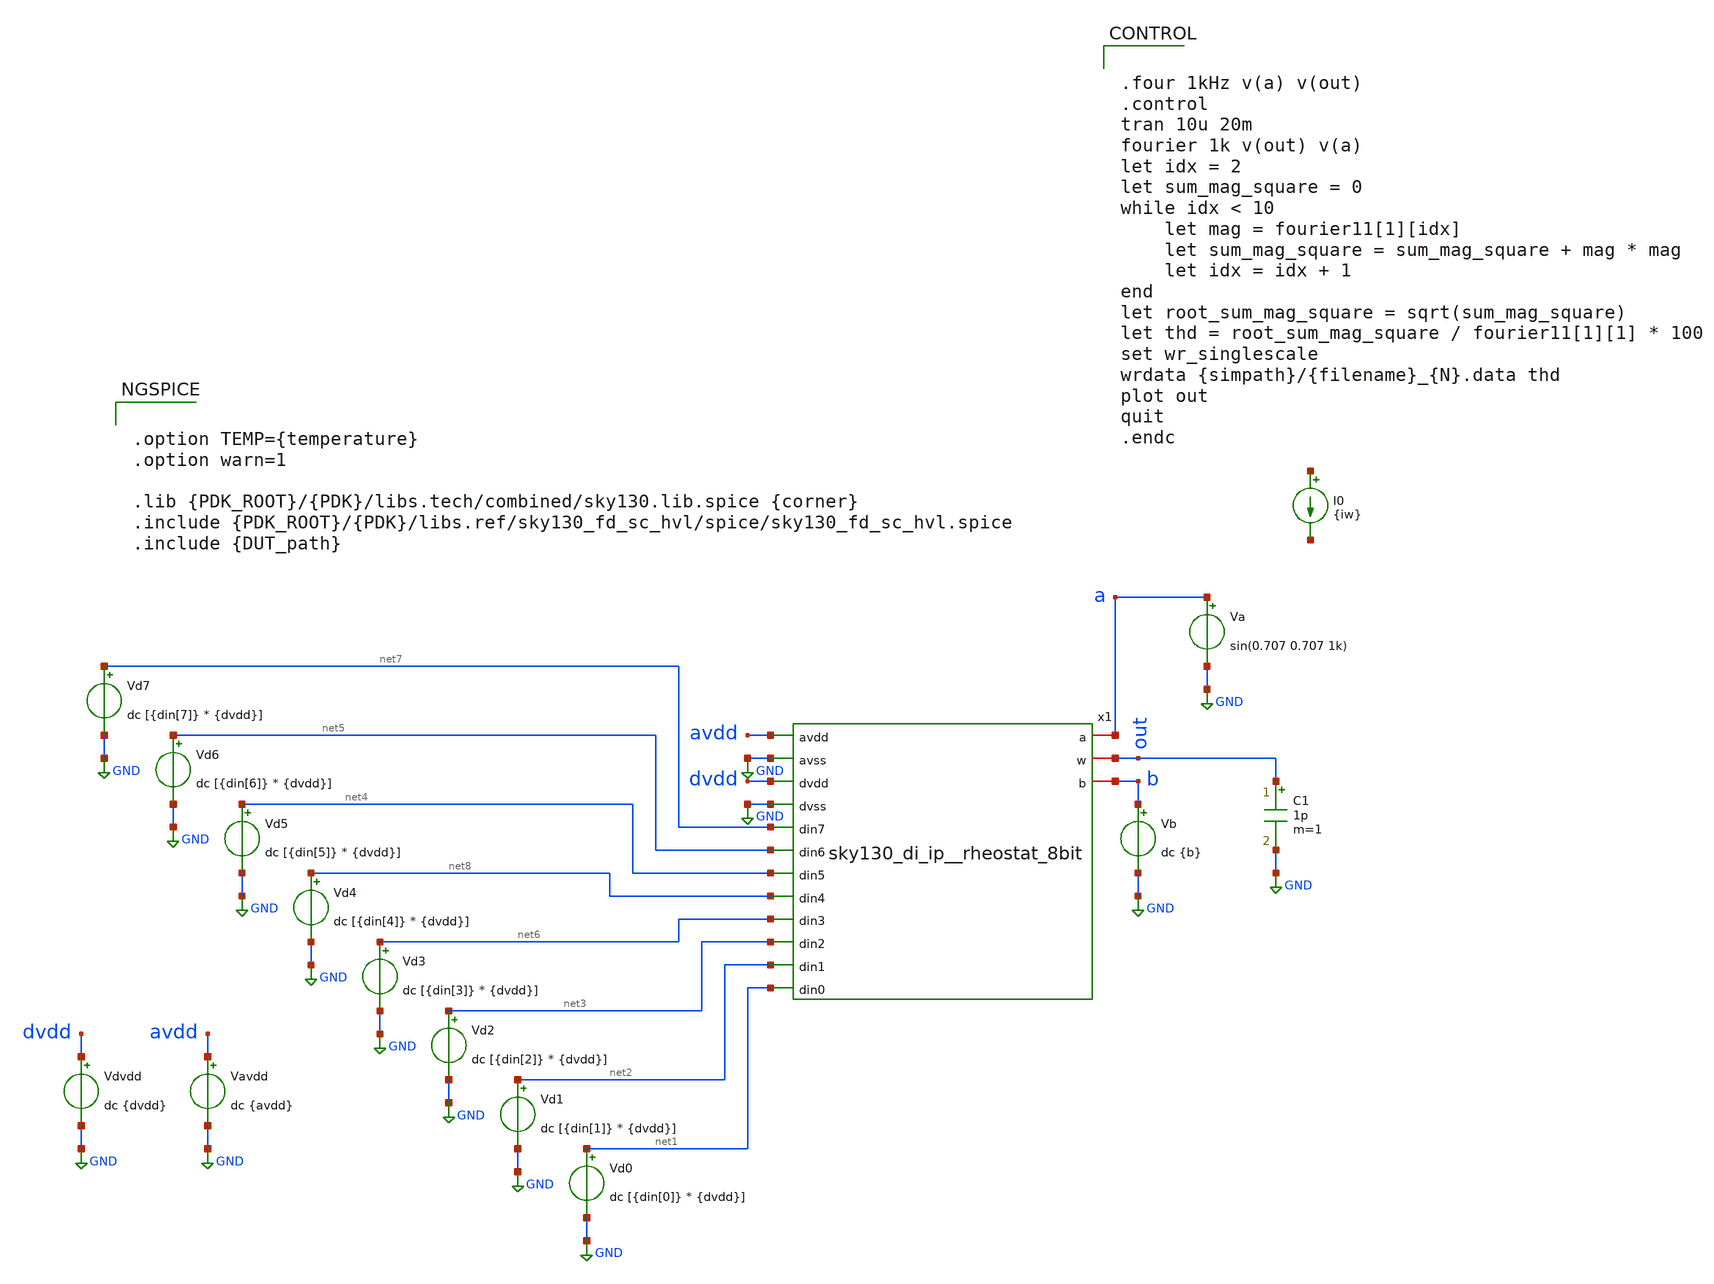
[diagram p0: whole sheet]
** sch_path: cace/tb_thd.sch
**.subckt tb_thd
x1 avdd GND dvdd GND net7 net5 net4 a net8 net6 out net3 net2 net1 b sky130_di_ip__rheostat_8bit
Vd0 net1 GND dc [{din[0]} * {dvdd}]
Vd1 net2 GND dc [{din[1]} * {dvdd}]
Vd2 net3 GND dc [{din[2]} * {dvdd}]
Vd3 net6 GND dc [{din[3]} * {dvdd}]
Vd4 net8 GND dc [{din[4]} * {dvdd}]
Vd5 net4 GND dc [{din[5]} * {dvdd}]
Vd6 net5 GND dc [{din[6]} * {dvdd}]
Vd7 net7 GND dc [{din[7]} * {dvdd}]
Vdvdd dvdd GND dc {dvdd}
Vavdd avdd GND dc {avdd}
Va a GND sin(0.707 0.707 1k)
Vb b GND dc {b}
I0 net9 net10 {iw}
C1 out GND 1p m=1
**** begin user architecture code


.option TEMP={temperature}
.option warn=1

.lib {PDK_ROOT}/{PDK}/libs.tech/combined/sky130.lib.spice {corner}
.include {PDK_ROOT}/{PDK}/libs.ref/sky130_fd_sc_hvl/spice/sky130_fd_sc_hvl.spice
.include {DUT_path}




.four 1kHz v(a) v(out)
.control
tran 10u 20m
fourier 1k v(out) v(a)
let idx = 2
let sum_mag_square = 0
while idx < 10
    let mag = fourier11[1][idx]
    let sum_mag_square = sum_mag_square + mag * mag
    let idx = idx + 1
end
let root_sum_mag_square = sqrt(sum_mag_square)
let thd = root_sum_mag_square / fourier11[1][1] * 100
set wr_singlescale
wrdata {simpath}/{filename}_{N}.data thd
plot out
quit
.endc




.subckt sky130_fd_sc_hvl__inv_1 A VGND VNB VPB VPWR Y
X0 VPWR A Y VPB sky130_fd_pr__pfet_g5v0d10v5 w=1.5e+06u l=500000u
X1 VGND A Y VNB sky130_fd_pr__nfet_g5v0d10v5 w=750000u l=500000u
.ends

.subckt sky130_fd_sc_hvl__lsbuflv2hv_1 A LVPWR VGND VNB VPB VPWR X
X0 VGND a_404_1133# a_504_1221# VNB sky130_fd_pr__nfet_g5v0d10v5 w=1.5e+06u l=500000u
X1 a_504_1221# a_404_1133# VGND VNB sky130_fd_pr__nfet_g5v0d10v5 w=1.5e+06u l=500000u
X2 X a_1711_885# VPWR VPB sky130_fd_pr__pfet_g5v0d10v5 w=1.5e+06u l=500000u
X3 X a_1711_885# VGND VNB sky130_fd_pr__nfet_g5v0d10v5 w=750000u l=500000u
X4 VGND A a_404_1133# VNB sky130_fd_pr__nfet_01v8 w=840000u l=150000u
X5 a_1197_107# a_772_151# VGND VNB sky130_fd_pr__nfet_g5v0d10v5 w=1.5e+06u l=500000u
X6 VPWR a_1197_107# a_504_1221# VPB sky130_fd_pr__pfet_g5v0d10v5 w=420000u l=1e+06u
X7 a_504_1221# a_404_1133# VGND VNB sky130_fd_pr__nfet_g5v0d10v5 w=1.5e+06u l=500000u
X8 a_1197_107# a_772_151# VGND VNB sky130_fd_pr__nfet_g5v0d10v5 w=1.5e+06u l=500000u
X9 a_772_151# a_404_1133# VGND VNB sky130_fd_pr__nfet_01v8 w=840000u l=150000u
X10 a_504_1221# a_404_1133# VGND VNB sky130_fd_pr__nfet_g5v0d10v5 w=1.5e+06u l=500000u
X11 VGND a_404_1133# a_504_1221# VNB sky130_fd_pr__nfet_g5v0d10v5 w=1.5e+06u l=500000u
X12 LVPWR A a_404_1133# LVPWR sky130_fd_pr__pfet_01v8_hvt w=840000u l=150000u
X13 VGND a_772_151# a_1197_107# VNB sky130_fd_pr__nfet_g5v0d10v5 w=1.5e+06u l=500000u
X14 VPWR a_504_1221# a_1711_885# VPB sky130_fd_pr__pfet_g5v0d10v5 w=1.5e+06u l=500000u
X15 VGND a_504_1221# a_1711_885# VNB sky130_fd_pr__nfet_g5v0d10v5 w=750000u l=500000u
X16 VGND a_772_151# a_1197_107# VNB sky130_fd_pr__nfet_g5v0d10v5 w=1.5e+06u l=500000u
X17 a_772_151# a_404_1133# LVPWR LVPWR sky130_fd_pr__pfet_01v8_hvt w=840000u l=150000u
X18 a_1197_107# a_772_151# VGND VNB sky130_fd_pr__nfet_g5v0d10v5 w=1.5e+06u l=500000u
X19 VPWR a_504_1221# a_1197_107# VPB sky130_fd_pr__pfet_g5v0d10v5 w=420000u l=1e+06u
.ends


**** end user architecture code
**.ends
.GLOBAL GND
.end
